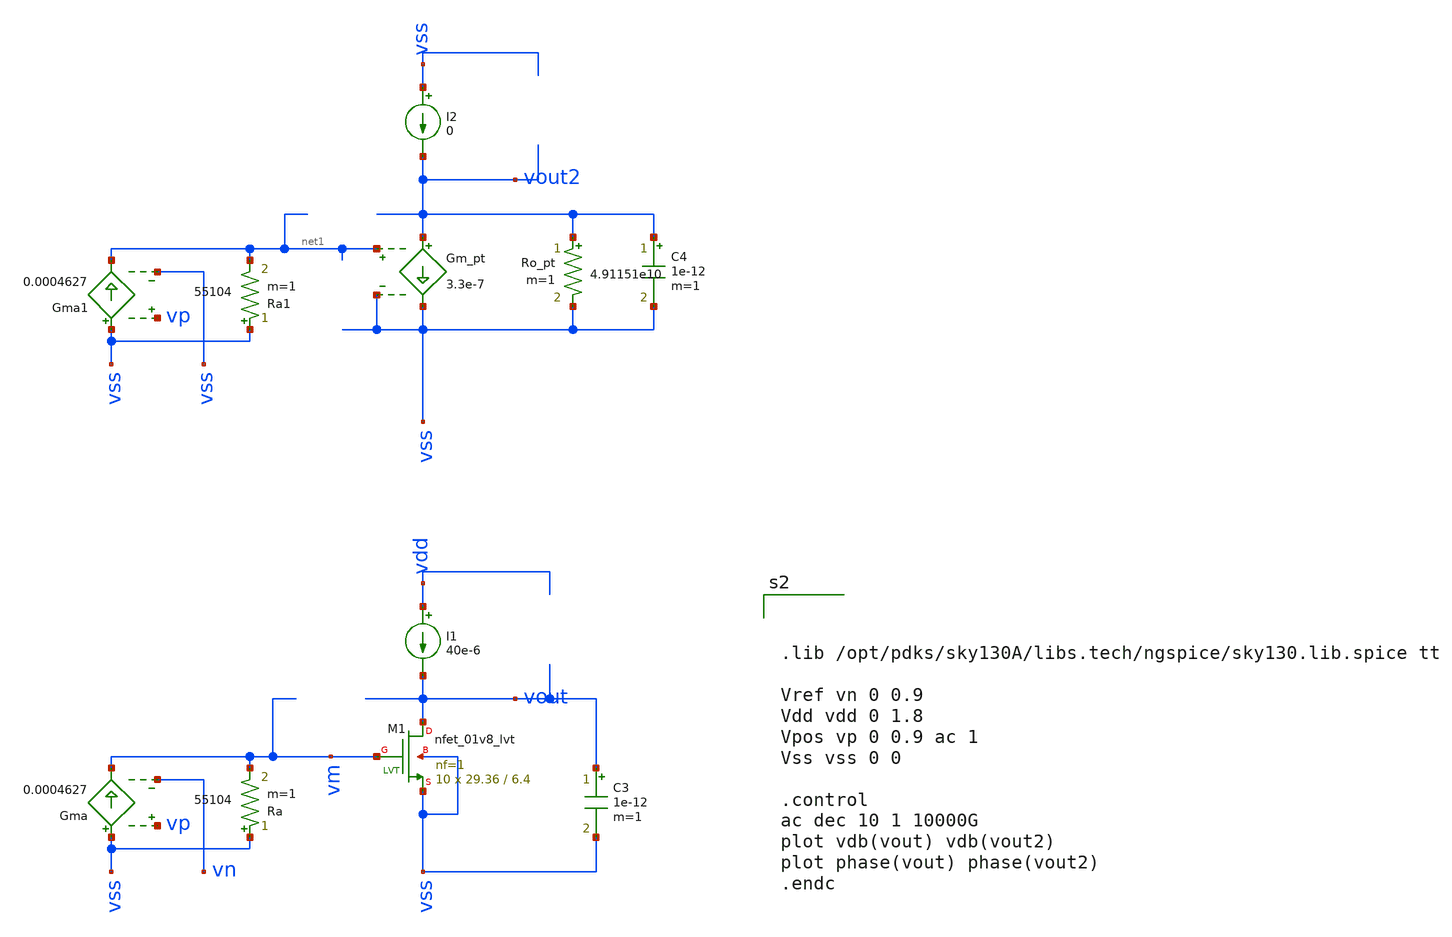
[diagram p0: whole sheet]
** sch_path: test/sstadex/xschem/1_cmos.sch
**.subckt 1_cmos
I1 vdd vout 40e-6
Gma vss vm vp vn 0.0004627
Ra vss vm 55104 m=1
Gma1 vss net1 vp vss 0.0004627
Ra1 vss net1 55104 m=1
Ro_pt vout2 vss 4.91151e10 m=1
Gm_pt vout2 vss net1 vss 3.3e-7
I2 vss vout2 0
XM1 vout vm vss vss sky130_fd_pr__nfet_01v8_lvt L=6.4 W=29.36 nf=1 ad='int((nf+1)/2) * W/nf * 0.29' as='int((nf+2)/2) * W/nf * 0.29'
+ pd='2*int((nf+1)/2) * (W/nf + 0.29)' ps='2*int((nf+2)/2) * (W/nf + 0.29)' nrd='0.29 / W' nrs='0.29 / W'
+ sa=0 sb=0 sd=0 mult=10 m=10
C3 vout vss 1e-12 m=1
C4 vout2 vss 1e-12 m=1
**** begin user architecture code



.lib /opt/pdks/sky130A/libs.tech/ngspice/sky130.lib.spice tt

Vref vn 0 0.9
Vdd vdd 0 1.8
Vpos vp 0 0.9 ac 1
Vss vss 0 0

.control
ac dec 10 1 10000G
plot vdb(vout) vdb(vout2)
plot phase(vout) phase(vout2)
.endc




**** end user architecture code
**.ends
.end
